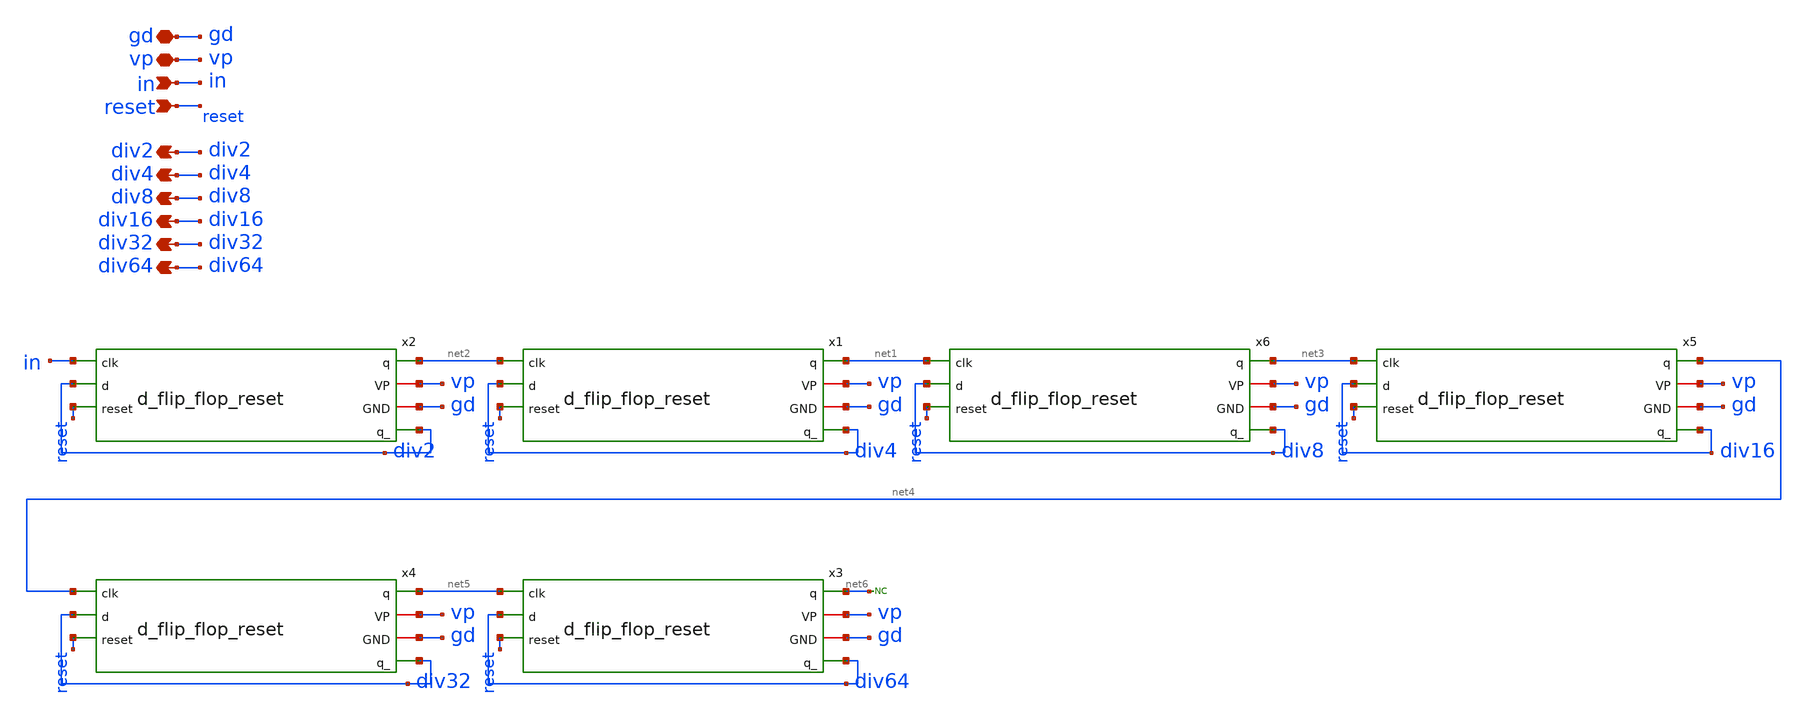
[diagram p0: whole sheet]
** sch_path: schematics/divider/schematics/div_with_reset.sch
**.subckt div_with_reset gd in vp div2 div4 div8 div16 div32 div64 reset
*.iopin gd
*.ipin in
*.iopin vp
*.opin div2
*.opin div4
*.opin div8
*.opin div16
*.opin div32
*.opin div64
*.ipin reset
x1 net1 vp gd div4 net2 div4 reset d_flip_flop_reset
x2 net2 vp gd div2 in div2 reset d_flip_flop_reset
x3 net6 vp gd div64 net5 div64 reset d_flip_flop_reset
x4 net5 vp gd div32 net4 div32 reset d_flip_flop_reset
x5 net4 vp gd div16 net3 div16 reset d_flip_flop_reset
x6 net3 vp gd div8 net1 div8 reset d_flip_flop_reset
* noconn #net6
**.ends
.end
